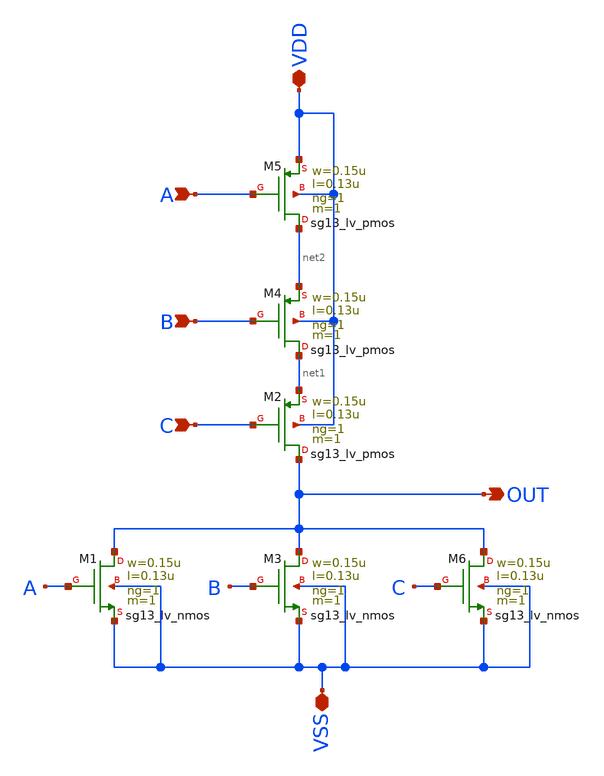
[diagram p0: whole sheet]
** sch_path: CDR4176-main/schematic/xschem/nor_x3_custom/nor_x3_custom.sch
**.subckt nor_x3_custom VDD VSS B C OUT A
*.iopin VDD
*.iopin VSS
*.ipin B
*.ipin C
*.opin OUT
*.ipin A
XM1 OUT A VSS VSS sg13_lv_nmos w=0.15u l=0.13u ng=1 m=1 mm_ok=1
XM2 OUT C net1 VDD sg13_lv_pmos w=0.15u l=0.13u ng=1 m=1 mm_ok=1
XM3 OUT B VSS VSS sg13_lv_nmos w=0.15u l=0.13u ng=1 m=1 mm_ok=1
XM4 net1 B net2 VDD sg13_lv_pmos w=0.15u l=0.13u ng=1 m=1 mm_ok=1
XM5 net2 A VDD VDD sg13_lv_pmos w=0.15u l=0.13u ng=1 m=1 mm_ok=1
XM6 OUT C VSS VSS sg13_lv_nmos w=0.15u l=0.13u ng=1 m=1 mm_ok=1
**.ends
.end
